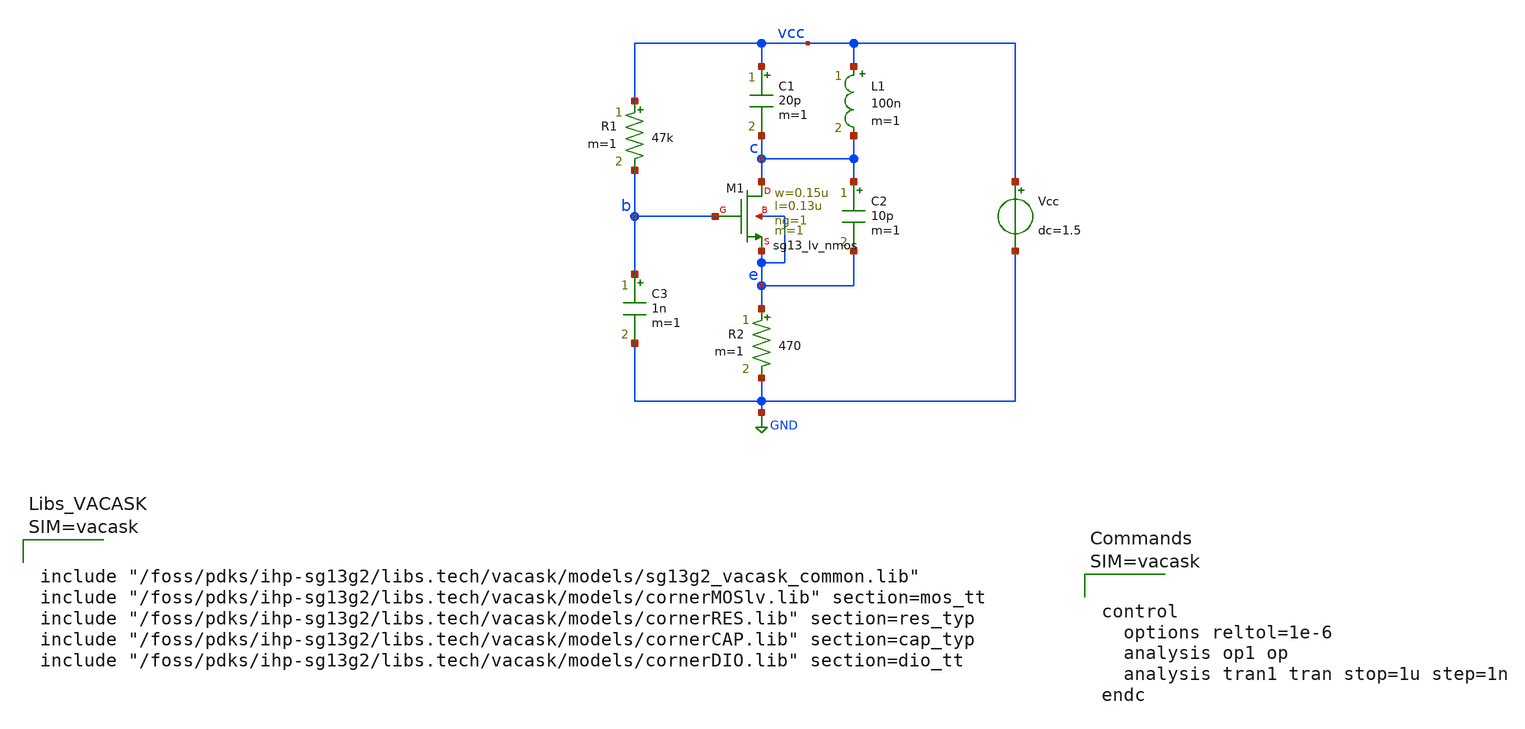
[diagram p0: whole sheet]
** sch_path: examples/source_follower/tb/vacask_demo.sch
**.subckt vacask_demo
R1 vcc b 47k m=1
R2 e GND 470 m=1
C1 vcc c 20p m=1
C2 c e 10p m=1
C3 b GND 1n m=1
L1 vcc c 100n m=1
Vcc vcc GND dc=1.5
XM1 c b e e sg13_lv_nmos w=0.15u l=0.13u ng=1 m=1 mm_ok=1
**** begin user architecture code






**** end user architecture code
**.ends
.GLOBAL GND
.end
